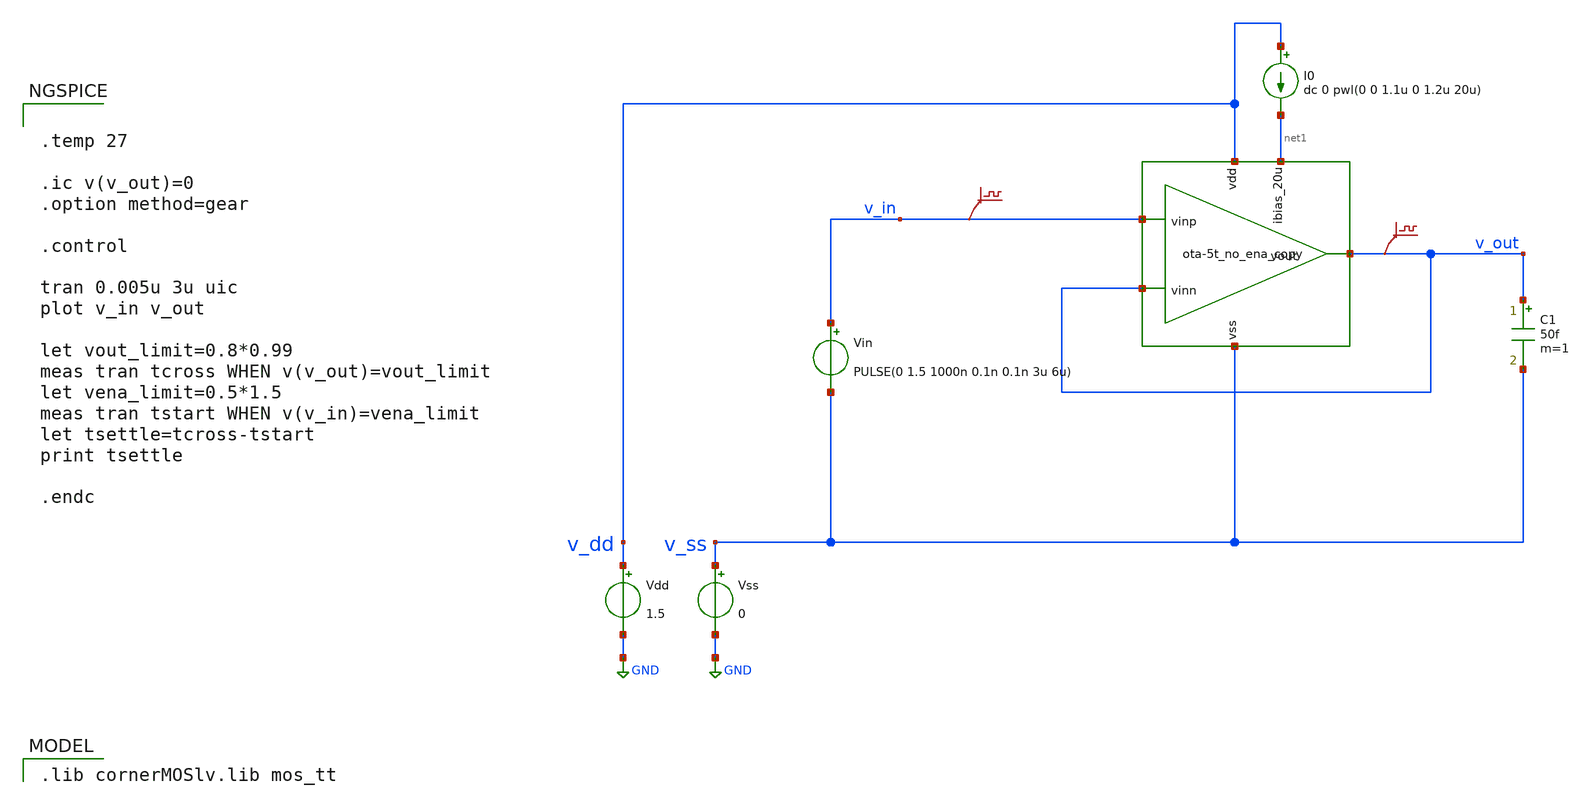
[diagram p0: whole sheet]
** sch_path: 004_Real_Circuits/003_version_second_output_stage/ota-5t_tb-tran_no_ena.sch
* (c) 2024-2025 Harald Pretl, Apache-2.0 license
**.subckt ota-5t_tb-tran_no_ena
Vdd v_dd GND 1.5
Vss v_ss GND 0
C1 v_out v_ss 50f m=1
Vin v_in v_ss PULSE(0 1.5 1000n 0.1n 0.1n 3u 6u)
I0 v_dd net1 dc 0 pwl(0 0 1.1u 0 1.2u 20u)
.save v(v_in)
.save v(v_out)
x1 v_dd v_out v_in v_out net1 v_ss ota-5t_no_ena_copy
**** begin user architecture code
 .lib cornerMOSlv.lib mos_tt



.temp 27

.ic v(v_out)=0
.option method=gear

.control

tran 0.005u 3u uic
plot v_in v_out

let vout_limit=0.8*0.99
meas tran tcross WHEN v(v_out)=vout_limit
let vena_limit=0.5*1.5
meas tran tstart WHEN v(v_in)=vena_limit
let tsettle=tcross-tstart
print tsettle

.endc


**** end user architecture code
**.ends

* expanding   symbol:  004_Real_Circuits/003_version_second_output_stage/ota-5t_no_ena_copy.sym # of
*+ pins=6
** sym_path: 004_Real_Circuits/003_version_second_output_stage/ota-5t_no_ena_copy.sym
** sch_path: 004_Real_Circuits/003_version_second_output_stage/ota-5t_no_ena_copy.sch
.subckt ota-5t_no_ena_copy vdd vout vinp vinn ibias_20u vss
*.opin vout
*.iopin vdd
*.ipin vinp
*.ipin vinn
*.ipin ibias_20u
*.iopin vss
XM5 tail ibias_20u vss vss sg13_lv_nmos w=1.5u l=5u ng=1 m=1 mm_ok=1
XM4 net1 gate_p vdd vdd sg13_lv_pmos w=3.5u l=5u ng=1 m=1 mm_ok=1
XM1 gate_p vinn tail vss sg13_lv_nmos w=2u l=5u ng=1 m=1 mm_ok=1
XM2 net1 vinp tail vss sg13_lv_nmos w=2u l=5u ng=1 m=1 mm_ok=1
XM3 gate_p gate_p vdd vdd sg13_lv_pmos w=3.5u l=5u ng=1 m=1 mm_ok=1
XM6 ibias_20u ibias_20u vss vss sg13_lv_nmos w=10u l=5u ng=5 m=1 mm_ok=1
XM7 vout net1 vdd vdd sg13_lv_pmos w=8.5u l=5u ng=1 m=1 mm_ok=1
XM8 vout ibias_20u vss vss sg13_lv_nmos w=0.75u l=5u ng=1 m=1 mm_ok=1
C2 net2 vout 950f m=1
R1 net1 net2 65k m=1
.ends

.GLOBAL GND
.end
